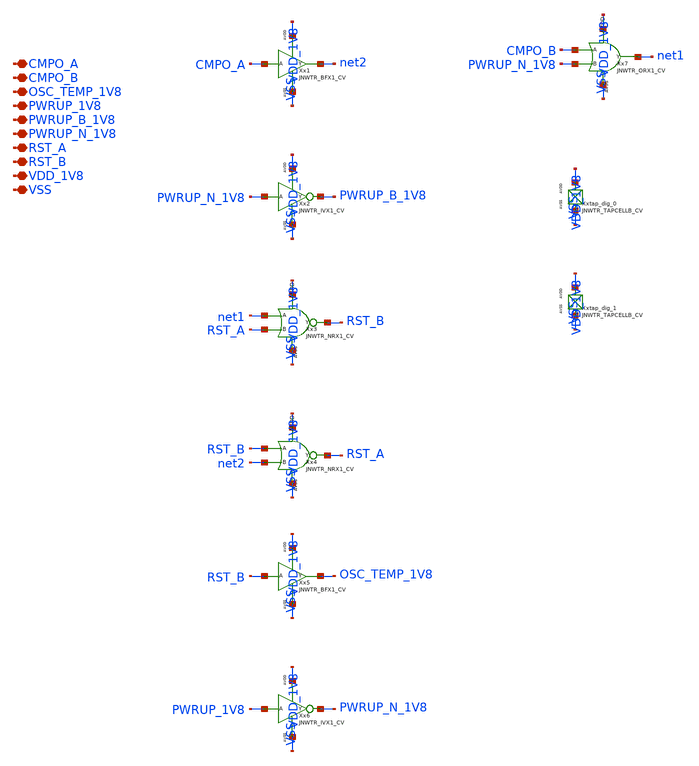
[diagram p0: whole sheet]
** sch_path: design/LELO_TEMP_SKY130A/LELO_TEMP_DIG.sch
**.subckt LELO_TEMP_DIG CMPO_A CMPO_B OSC_TEMP_1V8 PWRUP_1V8 PWRUP_B_1V8 PWRUP_N_1V8 RST_A RST_B
*+ VDD_1V8 VSS
*.iopin CMPO_A
*.iopin CMPO_B
*.iopin OSC_TEMP_1V8
*.iopin PWRUP_1V8
*.iopin PWRUP_B_1V8
*.iopin PWRUP_N_1V8
*.iopin RST_A
*.iopin RST_B
*.iopin VDD_1V8
*.iopin VSS
Xx2 PWRUP_N_1V8 PWRUP_B_1V8 VDD_1V8 VSS JNWTR_IVX1_CV
Xx3 net1 RST_A RST_B VDD_1V8 VSS JNWTR_NRX1_CV
Xx4 RST_B net2 RST_A VDD_1V8 VSS JNWTR_NRX1_CV
Xx6 PWRUP_1V8 PWRUP_N_1V8 VDD_1V8 VSS JNWTR_IVX1_CV
Xx7 CMPO_B PWRUP_N_1V8 net1 VDD_1V8 VSS JNWTR_ORX1_CV xoffset=0 yoffset=0 angle=0 M=1
Xxtap_dig_0 VDD_1V8 VSS JNWTR_TAPCELLB_CV xoffset=0 yoffset=0 angle=0
Xxtap_dig_1 VDD_1V8 VSS JNWTR_TAPCELLB_CV xoffset=0 yoffset=0 angle=0
**.ends
.end
